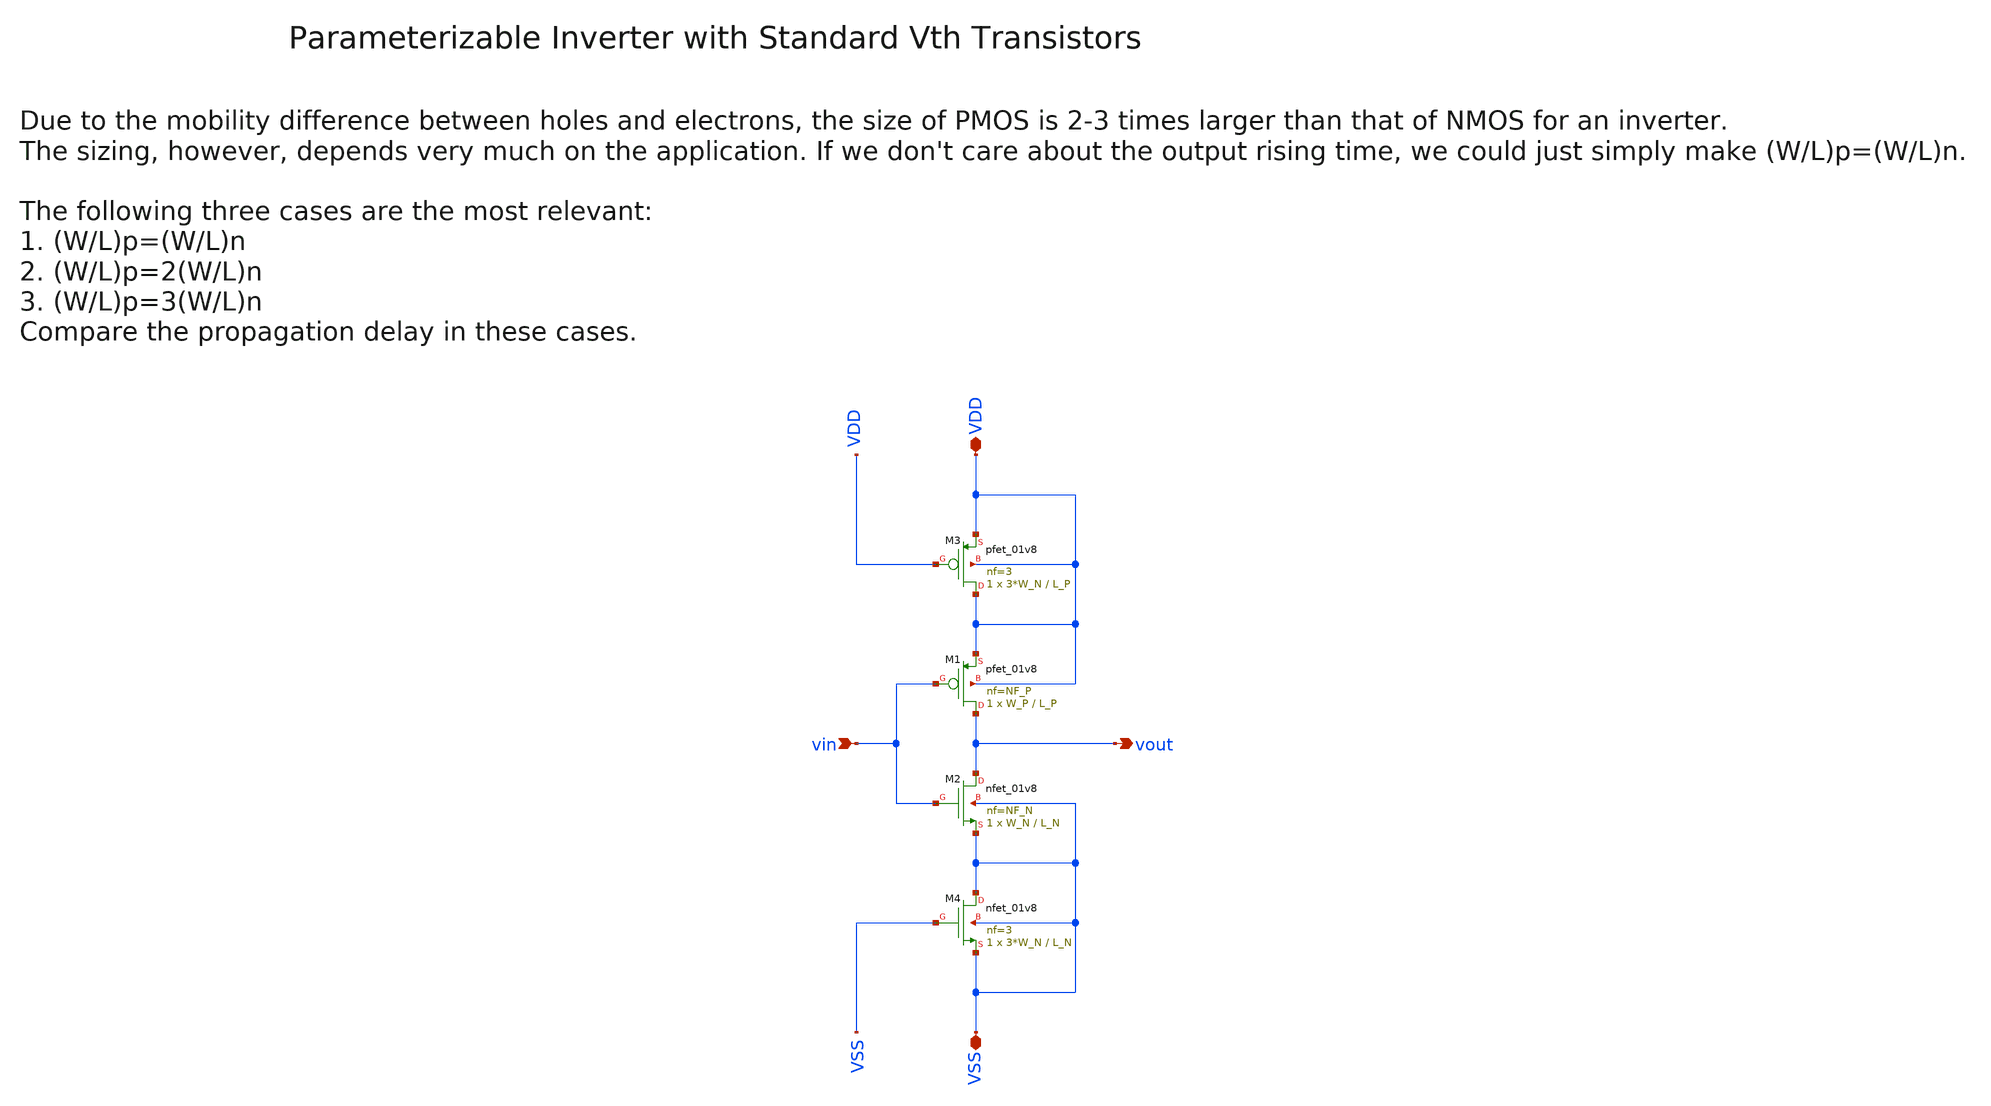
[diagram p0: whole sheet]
** sch_path: sky130/macros/iqmod/schematic/generic/wspr_tx_iqmod_mixer_lo_logic_inv_weak_gen.sch
**.subckt wspr_tx_iqmod_mixer_lo_logic_inv_weak_gen vin VDD VSS vout
*.ipin vin
*.iopin VDD
*.iopin VSS
*.opin vout
XM1 vout vin VDD VDD sky130_fd_pr__pfet_01v8 L=L_P W=W_P nf=NF_P ad='int((NF_P + 1)/2) * W_P / NF_P * 0.29'
+ as='int((NF_P + 2)/2) * W_P / NF_P * 0.29' pd='2*int((NF_P + 1)/2) * (W_P / NF_P + 0.29)' ps='2*int((NF_P + 2)/2) * (W_P / NF_P + 0.29)'
+ nrd='0.29 / W_P ' nrs='0.29 / W_P ' sa=0 sb=0 sd=0 mult=1 m=1
XM3 VDD VDD VDD VDD sky130_fd_pr__pfet_01v8 L=L_P W=3*W_N nf=3 ad='int((3 + 1)/2) * 3*W_N / 3 * 0.29'
+ as='int((3 + 2)/2) * 3*W_N / 3 * 0.29' pd='2*int((3 + 1)/2) * (3*W_N / 3 + 0.29)' ps='2*int((3 + 2)/2) * (3*W_N / 3 + 0.29)'
+ nrd='0.29 / 3*W_N ' nrs='0.29 / 3*W_N ' sa=0 sb=0 sd=0 mult=1 m=1
XM2 vout vin VSS VSS sky130_fd_pr__nfet_01v8 L=L_N W=W_N nf=NF_N ad='int((NF_N + 1)/2) * W_N / NF_N * 0.29'
+ as='int((NF_N + 2)/2) * W_N / NF_N * 0.29' pd='2*int((NF_N + 1)/2) * (W_N / NF_N + 0.29)' ps='2*int((NF_N + 2)/2) * (W_N / NF_N + 0.29)'
+ nrd='0.29 / W_N ' nrs='0.29 / W_N ' sa=0 sb=0 sd=0 mult=1 m=1
XM4 VSS VSS VSS VSS sky130_fd_pr__nfet_01v8 L=L_N W=3*W_N nf=3 ad='int((3 + 1)/2) * 3*W_N / 3 * 0.29'
+ as='int((3 + 2)/2) * 3*W_N / 3 * 0.29' pd='2*int((3 + 1)/2) * (3*W_N / 3 + 0.29)' ps='2*int((3 + 2)/2) * (3*W_N / 3 + 0.29)'
+ nrd='0.29 / 3*W_N ' nrs='0.29 / 3*W_N ' sa=0 sb=0 sd=0 mult=1 m=1
**.ends
.end
